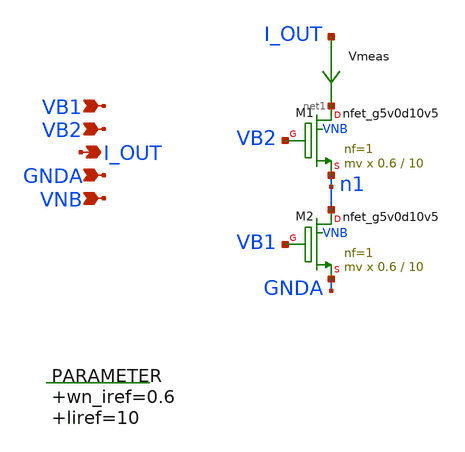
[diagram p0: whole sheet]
** sch_path: xschem/tail.sch
**.subckt tail I_OUT VB1 VB2 GNDA VNB
*.opin I_OUT
*.ipin VB1
*.ipin VB2
*.ipin GNDA
*.ipin VNB
.param wn_iref=0.6 liref=10

XM1 net1 VB2 n1 VNB sky130_fd_pr__nfet_g5v0d10v5 L=10 W=0.6 nf=1 ad='int((nf+1)/2) * W/nf * 0.29' as='int((nf+2)/2) * W/nf * 0.29'
+ pd='2*int((nf+1)/2) * (W/nf + 0.29)' ps='2*int((nf+2)/2) * (W/nf + 0.29)' nrd='0.29 / W' nrs='0.29 / W'
+ sa=0 sb=0 sd=0 mult=mv m=mv
Vmeas I_OUT net1 0
.save i(vmeas)
XM2 n1 VB1 GNDA VNB sky130_fd_pr__nfet_g5v0d10v5 L=10 W=0.6 nf=1 ad='int((nf+1)/2) * W/nf * 0.29' as='int((nf+2)/2) * W/nf * 0.29'
+ pd='2*int((nf+1)/2) * (W/nf + 0.29)' ps='2*int((nf+2)/2) * (W/nf + 0.29)' nrd='0.29 / W' nrs='0.29 / W'
+ sa=0 sb=0 sd=0 mult=mv m=mv
**.ends
.end
